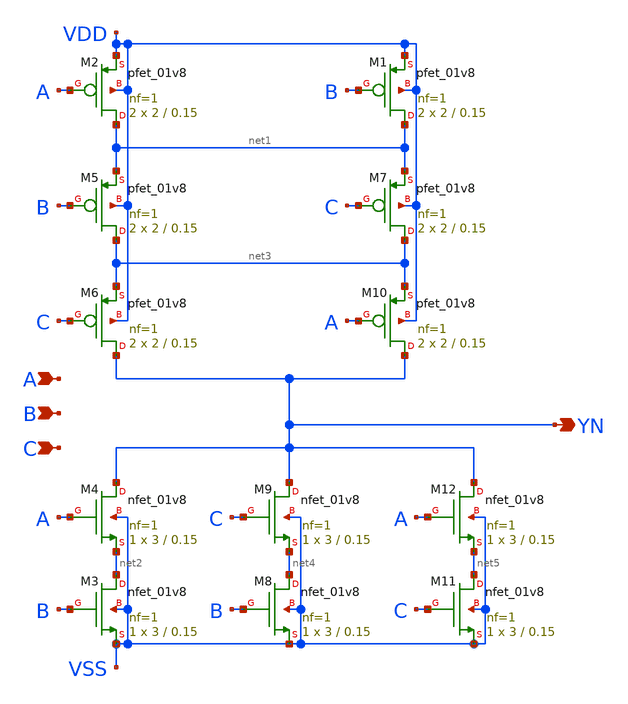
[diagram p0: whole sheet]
** sch_path: lib/xschem/VOTERN3X1.sch
**.subckt VOTERN3X1 YN A B C
*.opin YN
*.ipin A
*.ipin B
*.ipin C
XM2 net1 A VDD VDD sky130_fd_pr__pfet_01v8 L=0.15 W=2 nf=1 ad='int((nf+1)/2) * W/nf * 0.29' as='int((nf+2)/2) * W/nf * 0.29'
+ pd='2*int((nf+1)/2) * (W/nf + 0.29)' ps='2*int((nf+2)/2) * (W/nf + 0.29)' nrd='0.29 / W' nrs='0.29 / W'
+ sa=0 sb=0 sd=0 mult=2 m=2
XM3 net2 B VSS VSS sky130_fd_pr__nfet_01v8 L=0.15 W=3 nf=1 ad='int((nf+1)/2) * W/nf * 0.29' as='int((nf+2)/2) * W/nf * 0.29'
+ pd='2*int((nf+1)/2) * (W/nf + 0.29)' ps='2*int((nf+2)/2) * (W/nf + 0.29)' nrd='0.29 / W' nrs='0.29 / W'
+ sa=0 sb=0 sd=0 mult=1 m=1
XM4 YN A net2 VSS sky130_fd_pr__nfet_01v8 L=0.15 W=3 nf=1 ad='int((nf+1)/2) * W/nf * 0.29' as='int((nf+2)/2) * W/nf * 0.29'
+ pd='2*int((nf+1)/2) * (W/nf + 0.29)' ps='2*int((nf+2)/2) * (W/nf + 0.29)' nrd='0.29 / W' nrs='0.29 / W'
+ sa=0 sb=0 sd=0 mult=1 m=1
XM1 net1 B VDD VDD sky130_fd_pr__pfet_01v8 L=0.15 W=2 nf=1 ad='int((nf+1)/2) * W/nf * 0.29' as='int((nf+2)/2) * W/nf * 0.29'
+ pd='2*int((nf+1)/2) * (W/nf + 0.29)' ps='2*int((nf+2)/2) * (W/nf + 0.29)' nrd='0.29 / W' nrs='0.29 / W'
+ sa=0 sb=0 sd=0 mult=2 m=2
XM5 net3 B net1 VDD sky130_fd_pr__pfet_01v8 L=0.15 W=2 nf=1 ad='int((nf+1)/2) * W/nf * 0.29' as='int((nf+2)/2) * W/nf * 0.29'
+ pd='2*int((nf+1)/2) * (W/nf + 0.29)' ps='2*int((nf+2)/2) * (W/nf + 0.29)' nrd='0.29 / W' nrs='0.29 / W'
+ sa=0 sb=0 sd=0 mult=2 m=2
XM6 YN C net3 VDD sky130_fd_pr__pfet_01v8 L=0.15 W=2 nf=1 ad='int((nf+1)/2) * W/nf * 0.29' as='int((nf+2)/2) * W/nf * 0.29'
+ pd='2*int((nf+1)/2) * (W/nf + 0.29)' ps='2*int((nf+2)/2) * (W/nf + 0.29)' nrd='0.29 / W' nrs='0.29 / W'
+ sa=0 sb=0 sd=0 mult=2 m=2
XM7 net3 C net1 VDD sky130_fd_pr__pfet_01v8 L=0.15 W=2 nf=1 ad='int((nf+1)/2) * W/nf * 0.29' as='int((nf+2)/2) * W/nf * 0.29'
+ pd='2*int((nf+1)/2) * (W/nf + 0.29)' ps='2*int((nf+2)/2) * (W/nf + 0.29)' nrd='0.29 / W' nrs='0.29 / W'
+ sa=0 sb=0 sd=0 mult=2 m=2
XM10 YN A net3 VDD sky130_fd_pr__pfet_01v8 L=0.15 W=2 nf=1 ad='int((nf+1)/2) * W/nf * 0.29' as='int((nf+2)/2) * W/nf * 0.29'
+ pd='2*int((nf+1)/2) * (W/nf + 0.29)' ps='2*int((nf+2)/2) * (W/nf + 0.29)' nrd='0.29 / W' nrs='0.29 / W'
+ sa=0 sb=0 sd=0 mult=2 m=2
XM8 net4 B VSS VSS sky130_fd_pr__nfet_01v8 L=0.15 W=3 nf=1 ad='int((nf+1)/2) * W/nf * 0.29' as='int((nf+2)/2) * W/nf * 0.29'
+ pd='2*int((nf+1)/2) * (W/nf + 0.29)' ps='2*int((nf+2)/2) * (W/nf + 0.29)' nrd='0.29 / W' nrs='0.29 / W'
+ sa=0 sb=0 sd=0 mult=1 m=1
XM9 YN C net4 VSS sky130_fd_pr__nfet_01v8 L=0.15 W=3 nf=1 ad='int((nf+1)/2) * W/nf * 0.29' as='int((nf+2)/2) * W/nf * 0.29'
+ pd='2*int((nf+1)/2) * (W/nf + 0.29)' ps='2*int((nf+2)/2) * (W/nf + 0.29)' nrd='0.29 / W' nrs='0.29 / W'
+ sa=0 sb=0 sd=0 mult=1 m=1
XM11 net5 C VSS VSS sky130_fd_pr__nfet_01v8 L=0.15 W=3 nf=1 ad='int((nf+1)/2) * W/nf * 0.29' as='int((nf+2)/2) * W/nf * 0.29'
+ pd='2*int((nf+1)/2) * (W/nf + 0.29)' ps='2*int((nf+2)/2) * (W/nf + 0.29)' nrd='0.29 / W' nrs='0.29 / W'
+ sa=0 sb=0 sd=0 mult=1 m=1
XM12 YN A net5 VSS sky130_fd_pr__nfet_01v8 L=0.15 W=3 nf=1 ad='int((nf+1)/2) * W/nf * 0.29' as='int((nf+2)/2) * W/nf * 0.29'
+ pd='2*int((nf+1)/2) * (W/nf + 0.29)' ps='2*int((nf+2)/2) * (W/nf + 0.29)' nrd='0.29 / W' nrs='0.29 / W'
+ sa=0 sb=0 sd=0 mult=1 m=1
**.ends
.end
